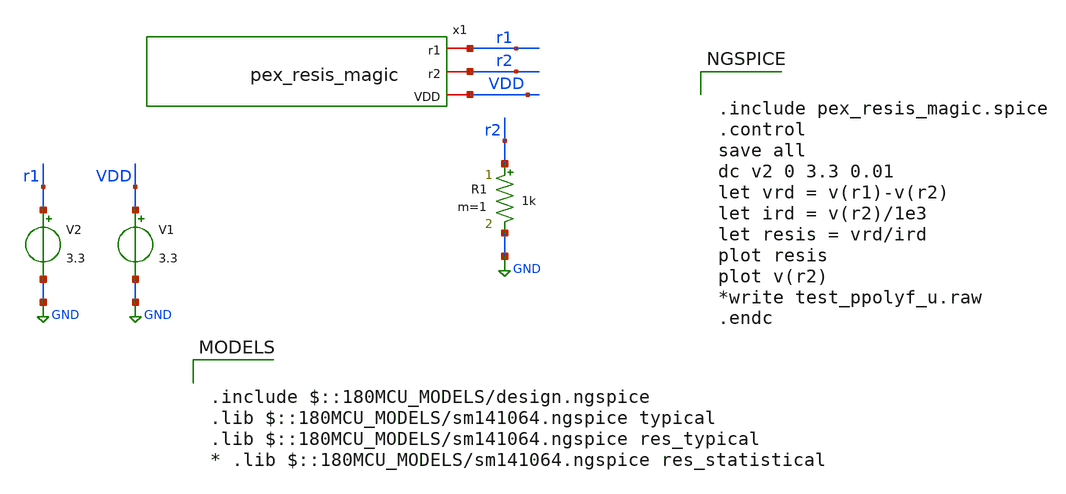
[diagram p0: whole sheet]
** sch_path: SCOP_INPUT_AND_MUX_PAKISTAN_03/Xschem/resistor_divider/resis_TB.sch
**.subckt resis_TB
V1 VDD GND 3.3
V2 r1 GND 3.3
R1 r2 GND 1k m=1
x1 r1 r2 VDD pex_resis_magic
**** begin user architecture code

.include $::180MCU_MODELS/design.ngspice
.lib $::180MCU_MODELS/sm141064.ngspice typical
.lib $::180MCU_MODELS/sm141064.ngspice res_typical
* .lib $::180MCU_MODELS/sm141064.ngspice res_statistical



.include pex_resis_magic.spice
.control
save all
dc v2 0 3.3 0.01
let vrd = v(r1)-v(r2)
let ird = v(r2)/1e3
let resis = vrd/ird
plot resis
plot v(r2)
*write test_ppolyf_u.raw
.endc


**** end user architecture code
**.ends
.GLOBAL GND
.end
